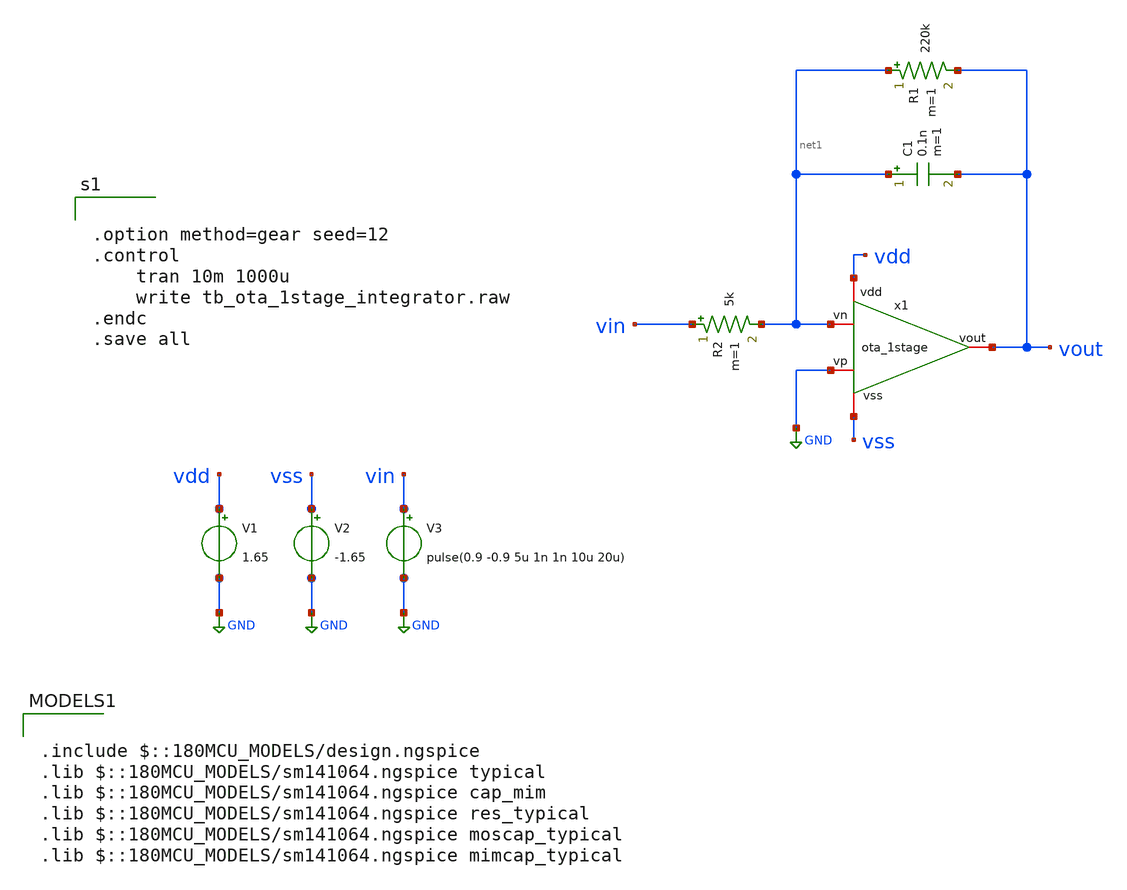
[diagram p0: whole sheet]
** sch_path: designs/libs/core_LIF_comp/tb_ota_1stage/tb_ota_1stage_integrator.sch
**.subckt tb_ota_1stage_integrator
V1 vdd GND 1.65
V3 vin GND pulse(0.9 -0.9 5u 1n 1n 10u 20u)
R1 net1 vout 220k m=1
C1 net1 vout 0.1n m=1
R2 vin net1 5k m=1
V2 vss GND -1.65
x1 vdd vout GND net1 vss ota_1stage
**** begin user architecture code


.option method=gear seed=12
.control
    tran 10m 1000u
    write tb_ota_1stage_integrator.raw
.endc
.save all



.include $::180MCU_MODELS/design.ngspice
.lib $::180MCU_MODELS/sm141064.ngspice typical
.lib $::180MCU_MODELS/sm141064.ngspice cap_mim
.lib $::180MCU_MODELS/sm141064.ngspice res_typical
.lib $::180MCU_MODELS/sm141064.ngspice moscap_typical
.lib $::180MCU_MODELS/sm141064.ngspice mimcap_typical

**** end user architecture code
**.ends

* expanding   symbol:  designs/libs/core_LIF_comp/core_ota_1stage/ota_1stage.sym # of pins=5
** sym_path: designs/libs/core_LIF_comp/core_ota_1stage/ota_1stage.sym
** sch_path: designs/libs/core_LIF_comp/core_ota_1stage/ota_1stage.sch
.subckt ota_1stage vdd vout vp vn vss
*.iopin vdd
*.iopin vss
*.iopin vp
*.iopin vn
*.iopin vout
XM1 net1 net1 vdd vdd pfet_03v3 L=0.28u W=0.84u nf=1 ad='int((nf+1)/2) * W/nf * 0.18u' as='int((nf+2)/2) * W/nf * 0.18u'
+ pd='2*int((nf+1)/2) * (W/nf + 0.18u)' ps='2*int((nf+2)/2) * (W/nf + 0.18u)' nrd='0.18u / W' nrs='0.18u / W'
+ sa=0 sb=0 sd=0 m=1
XM2 net1 vp net2 vss nfet_03v3 L=0.28u W=3.08u nf=1 ad='int((nf+1)/2) * W/nf * 0.18u' as='int((nf+2)/2) * W/nf * 0.18u'
+ pd='2*int((nf+1)/2) * (W/nf + 0.18u)' ps='2*int((nf+2)/2) * (W/nf + 0.18u)' nrd='0.18u / W' nrs='0.18u / W'
+ sa=0 sb=0 sd=0 m=1
XM4 vout net1 vdd vdd pfet_03v3 L=0.28u W=0.84u nf=1 ad='int((nf+1)/2) * W/nf * 0.18u' as='int((nf+2)/2) * W/nf * 0.18u'
+ pd='2*int((nf+1)/2) * (W/nf + 0.18u)' ps='2*int((nf+2)/2) * (W/nf + 0.18u)' nrd='0.18u / W' nrs='0.18u / W'
+ sa=0 sb=0 sd=0 m=1
XM3 vout vn net2 vss nfet_03v3 L=0.28u W=3.08u nf=1 ad='int((nf+1)/2) * W/nf * 0.18u' as='int((nf+2)/2) * W/nf * 0.18u'
+ pd='2*int((nf+1)/2) * (W/nf + 0.18u)' ps='2*int((nf+2)/2) * (W/nf + 0.18u)' nrd='0.18u / W' nrs='0.18u / W'
+ sa=0 sb=0 sd=0 m=1
XM5 net2 net3 vss vss nfet_03v3 L=0.28u W=0.84u nf=1 ad='int((nf+1)/2) * W/nf * 0.18u' as='int((nf+2)/2) * W/nf * 0.18u'
+ pd='2*int((nf+1)/2) * (W/nf + 0.18u)' ps='2*int((nf+2)/2) * (W/nf + 0.18u)' nrd='0.18u / W' nrs='0.18u / W'
+ sa=0 sb=0 sd=0 m=1
XM6 net3 net3 vss vss nfet_03v3 L=0.28u W=0.84u nf=1 ad='int((nf+1)/2) * W/nf * 0.18u' as='int((nf+2)/2) * W/nf * 0.18u'
+ pd='2*int((nf+1)/2) * (W/nf + 0.18u)' ps='2*int((nf+2)/2) * (W/nf + 0.18u)' nrd='0.18u / W' nrs='0.18u / W'
+ sa=0 sb=0 sd=0 m=1
XM7 vdd vdd net3 vss nfet_03v3 L=8.54u W=0.28u nf=1 ad='int((nf+1)/2) * W/nf * 0.18u' as='int((nf+2)/2) * W/nf * 0.18u'
+ pd='2*int((nf+1)/2) * (W/nf + 0.18u)' ps='2*int((nf+2)/2) * (W/nf + 0.18u)' nrd='0.18u / W' nrs='0.18u / W'
+ sa=0 sb=0 sd=0 m=1
.ends

.GLOBAL GND
.end
